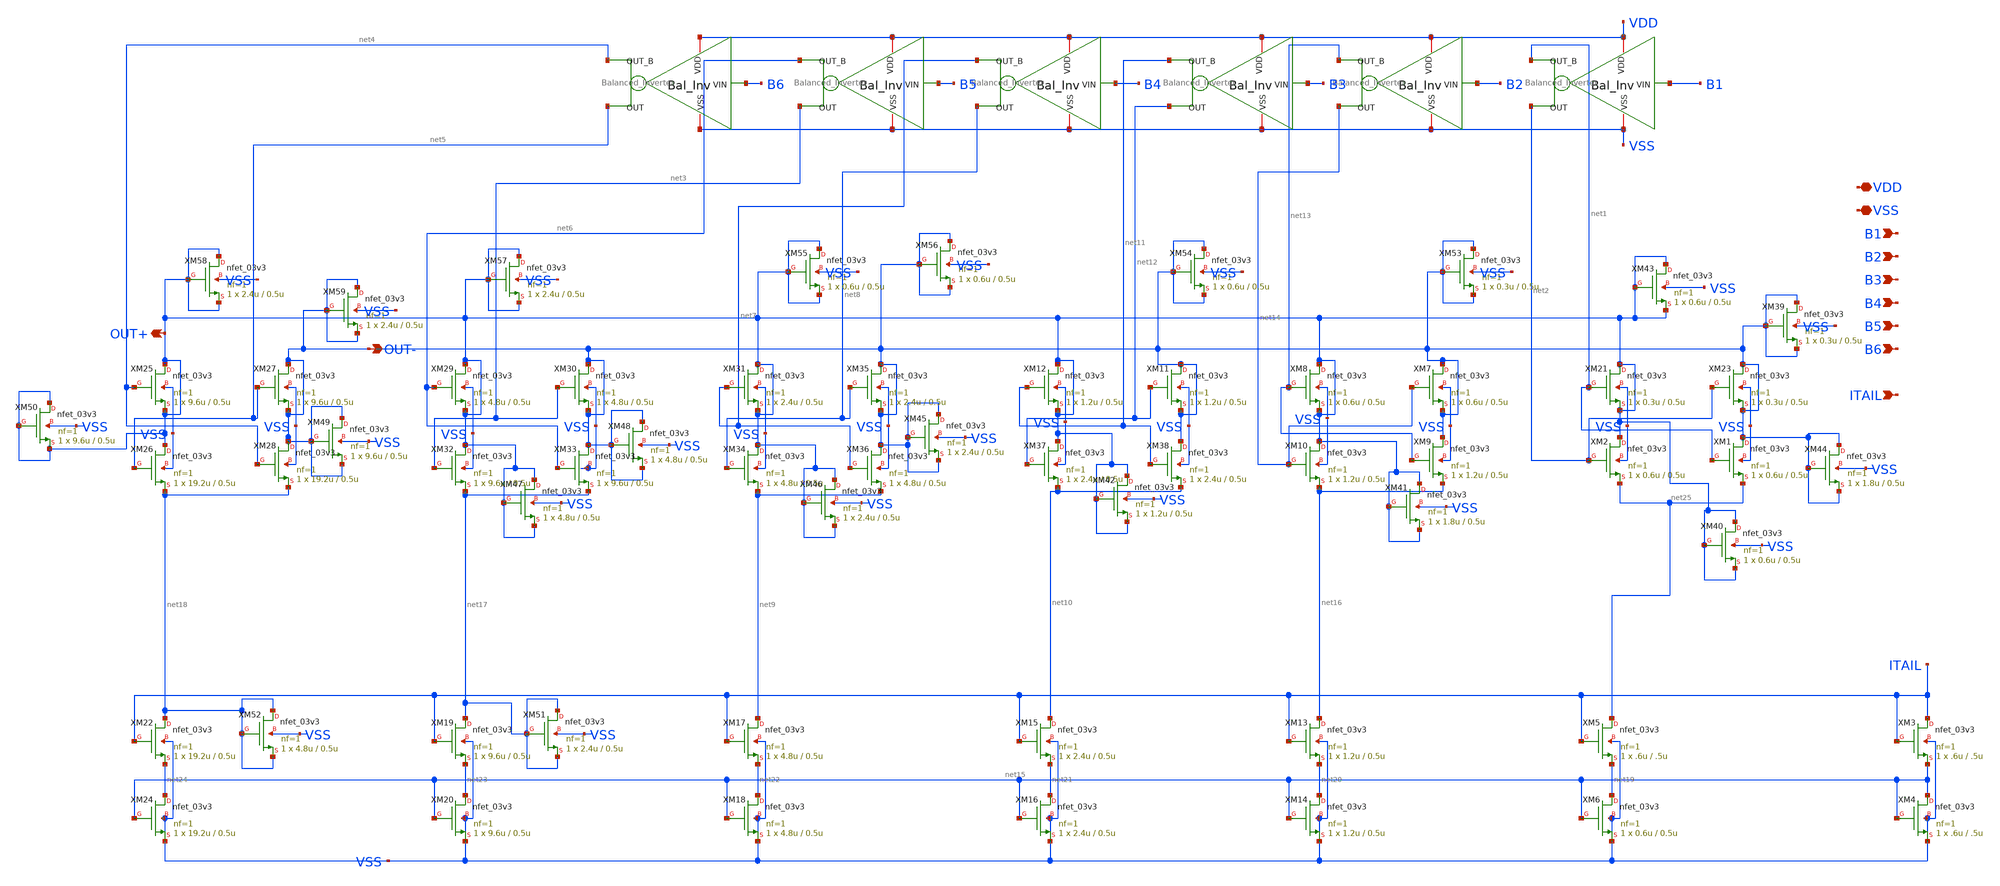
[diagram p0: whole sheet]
** sch_path: DAC_PAKISTAN_01/Pakistan1_Xschem/LSB_V1.sch
**.subckt LSB_V1 VDD VSS B1 B2 B3 B4 B5 B6 ITAIL OUT+ OUT-
*.iopin VDD
*.iopin VSS
*.ipin B1
*.ipin B2
*.ipin B3
*.ipin B4
*.ipin B5
*.ipin B6
*.ipin ITAIL
*.opin OUT+
*.opin OUT-
x1 VDD VSS B1 net1 net2 Balanced_Inverter
x2 VDD VSS B2 net13 net14 Balanced_Inverter
x3 VDD VSS B3 net11 net12 Balanced_Inverter
x4 VDD VSS B4 net7 net8 Balanced_Inverter
x5 VDD VSS B5 net6 net3 Balanced_Inverter
x6 VDD VSS B6 net4 net5 Balanced_Inverter
XM21 OUT+ net1 OUT+ VSS nfet_03v3 L=0.5u W=0.3u nf=1 ad='int((nf+1)/2) * W/nf * 0.18u' as='int((nf+2)/2) * W/nf * 0.18u'
+ pd='2*int((nf+1)/2) * (W/nf + 0.18u)' ps='2*int((nf+2)/2) * (W/nf + 0.18u)' nrd='0.18u / W' nrs='0.18u / W'
+ sa=0 sb=0 sd=0 m=1
XM23 OUT- net2 OUT- VSS nfet_03v3 L=0.5u W=0.3u nf=1 ad='int((nf+1)/2) * W/nf * 0.18u' as='int((nf+2)/2) * W/nf * 0.18u'
+ pd='2*int((nf+1)/2) * (W/nf + 0.18u)' ps='2*int((nf+2)/2) * (W/nf + 0.18u)' nrd='0.18u / W' nrs='0.18u / W'
+ sa=0 sb=0 sd=0 m=1
XM1 OUT- net1 net25 VSS nfet_03v3 L=0.5u W=0.6u nf=1 ad='int((nf+1)/2) * W/nf * 0.18u' as='int((nf+2)/2) * W/nf * 0.18u'
+ pd='2*int((nf+1)/2) * (W/nf + 0.18u)' ps='2*int((nf+2)/2) * (W/nf + 0.18u)' nrd='0.18u / W' nrs='0.18u / W'
+ sa=0 sb=0 sd=0 m=1
XM2 OUT+ net2 net25 VSS nfet_03v3 L=0.5u W=0.6u nf=1 ad='int((nf+1)/2) * W/nf * 0.18u' as='int((nf+2)/2) * W/nf * 0.18u'
+ pd='2*int((nf+1)/2) * (W/nf + 0.18u)' ps='2*int((nf+2)/2) * (W/nf + 0.18u)' nrd='0.18u / W' nrs='0.18u / W'
+ sa=0 sb=0 sd=0 m=1
XM3 ITAIL ITAIL net15 VSS nfet_03v3 L=.5u W=.6u nf=1 ad='int((nf+1)/2) * W/nf * 0.18u' as='int((nf+2)/2) * W/nf * 0.18u'
+ pd='2*int((nf+1)/2) * (W/nf + 0.18u)' ps='2*int((nf+2)/2) * (W/nf + 0.18u)' nrd='0.18u / W' nrs='0.18u / W'
+ sa=0 sb=0 sd=0 m=1
XM4 net15 net15 VSS VSS nfet_03v3 L=.5u W=.6u nf=1 ad='int((nf+1)/2) * W/nf * 0.18u' as='int((nf+2)/2) * W/nf * 0.18u'
+ pd='2*int((nf+1)/2) * (W/nf + 0.18u)' ps='2*int((nf+2)/2) * (W/nf + 0.18u)' nrd='0.18u / W' nrs='0.18u / W'
+ sa=0 sb=0 sd=0 m=1
XM5 net25 ITAIL net19 VSS nfet_03v3 L=.5u W=.6u nf=1 ad='int((nf+1)/2) * W/nf * 0.18u' as='int((nf+2)/2) * W/nf * 0.18u'
+ pd='2*int((nf+1)/2) * (W/nf + 0.18u)' ps='2*int((nf+2)/2) * (W/nf + 0.18u)' nrd='0.18u / W' nrs='0.18u / W'
+ sa=0 sb=0 sd=0 m=1
XM6 net19 net15 VSS VSS nfet_03v3 L=0.5u W=0.6u nf=1 ad='int((nf+1)/2) * W/nf * 0.18u' as='int((nf+2)/2) * W/nf * 0.18u'
+ pd='2*int((nf+1)/2) * (W/nf + 0.18u)' ps='2*int((nf+2)/2) * (W/nf + 0.18u)' nrd='0.18u / W' nrs='0.18u / W'
+ sa=0 sb=0 sd=0 m=1
XM7 OUT- net14 OUT- VSS nfet_03v3 L=0.5u W=0.6u nf=1 ad='int((nf+1)/2) * W/nf * 0.18u' as='int((nf+2)/2) * W/nf * 0.18u'
+ pd='2*int((nf+1)/2) * (W/nf + 0.18u)' ps='2*int((nf+2)/2) * (W/nf + 0.18u)' nrd='0.18u / W' nrs='0.18u / W'
+ sa=0 sb=0 sd=0 m=1
XM8 OUT+ net13 OUT+ VSS nfet_03v3 L=0.5u W=0.6u nf=1 ad='int((nf+1)/2) * W/nf * 0.18u' as='int((nf+2)/2) * W/nf * 0.18u'
+ pd='2*int((nf+1)/2) * (W/nf + 0.18u)' ps='2*int((nf+2)/2) * (W/nf + 0.18u)' nrd='0.18u / W' nrs='0.18u / W'
+ sa=0 sb=0 sd=0 m=1
XM9 OUT- net13 net16 VSS nfet_03v3 L=0.5u W=1.2u nf=1 ad='int((nf+1)/2) * W/nf * 0.18u' as='int((nf+2)/2) * W/nf * 0.18u'
+ pd='2*int((nf+1)/2) * (W/nf + 0.18u)' ps='2*int((nf+2)/2) * (W/nf + 0.18u)' nrd='0.18u / W' nrs='0.18u / W'
+ sa=0 sb=0 sd=0 m=1
XM10 OUT+ net14 net16 VSS nfet_03v3 L=0.5u W=1.2u nf=1 ad='int((nf+1)/2) * W/nf * 0.18u' as='int((nf+2)/2) * W/nf * 0.18u'
+ pd='2*int((nf+1)/2) * (W/nf + 0.18u)' ps='2*int((nf+2)/2) * (W/nf + 0.18u)' nrd='0.18u / W' nrs='0.18u / W'
+ sa=0 sb=0 sd=0 m=1
XM11 OUT- net12 OUT- VSS nfet_03v3 L=0.5u W=1.2u nf=1 ad='int((nf+1)/2) * W/nf * 0.18u' as='int((nf+2)/2) * W/nf * 0.18u'
+ pd='2*int((nf+1)/2) * (W/nf + 0.18u)' ps='2*int((nf+2)/2) * (W/nf + 0.18u)' nrd='0.18u / W' nrs='0.18u / W'
+ sa=0 sb=0 sd=0 m=1
XM12 OUT+ net11 OUT+ VSS nfet_03v3 L=0.5u W=1.2u nf=1 ad='int((nf+1)/2) * W/nf * 0.18u' as='int((nf+2)/2) * W/nf * 0.18u'
+ pd='2*int((nf+1)/2) * (W/nf + 0.18u)' ps='2*int((nf+2)/2) * (W/nf + 0.18u)' nrd='0.18u / W' nrs='0.18u / W'
+ sa=0 sb=0 sd=0 m=1
XM13 net16 ITAIL net20 VSS nfet_03v3 L=0.5u W=1.2u nf=1 ad='int((nf+1)/2) * W/nf * 0.18u' as='int((nf+2)/2) * W/nf * 0.18u'
+ pd='2*int((nf+1)/2) * (W/nf + 0.18u)' ps='2*int((nf+2)/2) * (W/nf + 0.18u)' nrd='0.18u / W' nrs='0.18u / W'
+ sa=0 sb=0 sd=0 m=1
XM14 net20 net15 VSS VSS nfet_03v3 L=0.5u W=1.2u nf=1 ad='int((nf+1)/2) * W/nf * 0.18u' as='int((nf+2)/2) * W/nf * 0.18u'
+ pd='2*int((nf+1)/2) * (W/nf + 0.18u)' ps='2*int((nf+2)/2) * (W/nf + 0.18u)' nrd='0.18u / W' nrs='0.18u / W'
+ sa=0 sb=0 sd=0 m=1
XM15 net10 ITAIL net21 VSS nfet_03v3 L=0.5u W=2.4u nf=1 ad='int((nf+1)/2) * W/nf * 0.18u' as='int((nf+2)/2) * W/nf * 0.18u'
+ pd='2*int((nf+1)/2) * (W/nf + 0.18u)' ps='2*int((nf+2)/2) * (W/nf + 0.18u)' nrd='0.18u / W' nrs='0.18u / W'
+ sa=0 sb=0 sd=0 m=1
XM16 net21 net15 VSS VSS nfet_03v3 L=0.5u W=2.4u nf=1 ad='int((nf+1)/2) * W/nf * 0.18u' as='int((nf+2)/2) * W/nf * 0.18u'
+ pd='2*int((nf+1)/2) * (W/nf + 0.18u)' ps='2*int((nf+2)/2) * (W/nf + 0.18u)' nrd='0.18u / W' nrs='0.18u / W'
+ sa=0 sb=0 sd=0 m=1
XM17 net9 ITAIL net22 VSS nfet_03v3 L=0.5u W=4.8u nf=1 ad='int((nf+1)/2) * W/nf * 0.18u' as='int((nf+2)/2) * W/nf * 0.18u'
+ pd='2*int((nf+1)/2) * (W/nf + 0.18u)' ps='2*int((nf+2)/2) * (W/nf + 0.18u)' nrd='0.18u / W' nrs='0.18u / W'
+ sa=0 sb=0 sd=0 m=1
XM18 net22 net15 VSS VSS nfet_03v3 L=0.5u W=4.8u nf=1 ad='int((nf+1)/2) * W/nf * 0.18u' as='int((nf+2)/2) * W/nf * 0.18u'
+ pd='2*int((nf+1)/2) * (W/nf + 0.18u)' ps='2*int((nf+2)/2) * (W/nf + 0.18u)' nrd='0.18u / W' nrs='0.18u / W'
+ sa=0 sb=0 sd=0 m=1
XM19 net17 ITAIL net23 VSS nfet_03v3 L=0.5u W=9.6u nf=1 ad='int((nf+1)/2) * W/nf * 0.18u' as='int((nf+2)/2) * W/nf * 0.18u'
+ pd='2*int((nf+1)/2) * (W/nf + 0.18u)' ps='2*int((nf+2)/2) * (W/nf + 0.18u)' nrd='0.18u / W' nrs='0.18u / W'
+ sa=0 sb=0 sd=0 m=1
XM20 net23 net15 VSS VSS nfet_03v3 L=0.5u W=9.6u nf=1 ad='int((nf+1)/2) * W/nf * 0.18u' as='int((nf+2)/2) * W/nf * 0.18u'
+ pd='2*int((nf+1)/2) * (W/nf + 0.18u)' ps='2*int((nf+2)/2) * (W/nf + 0.18u)' nrd='0.18u / W' nrs='0.18u / W'
+ sa=0 sb=0 sd=0 m=1
XM22 net18 ITAIL net24 VSS nfet_03v3 L=0.5u W=19.2u nf=1 ad='int((nf+1)/2) * W/nf * 0.18u' as='int((nf+2)/2) * W/nf * 0.18u'
+ pd='2*int((nf+1)/2) * (W/nf + 0.18u)' ps='2*int((nf+2)/2) * (W/nf + 0.18u)' nrd='0.18u / W' nrs='0.18u / W'
+ sa=0 sb=0 sd=0 m=1
XM24 net24 net15 VSS VSS nfet_03v3 L=0.5u W=19.2u nf=1 ad='int((nf+1)/2) * W/nf * 0.18u' as='int((nf+2)/2) * W/nf * 0.18u'
+ pd='2*int((nf+1)/2) * (W/nf + 0.18u)' ps='2*int((nf+2)/2) * (W/nf + 0.18u)' nrd='0.18u / W' nrs='0.18u / W'
+ sa=0 sb=0 sd=0 m=1
XM25 OUT+ net4 OUT+ VSS nfet_03v3 L=0.5u W=9.6u nf=1 ad='int((nf+1)/2) * W/nf * 0.18u' as='int((nf+2)/2) * W/nf * 0.18u'
+ pd='2*int((nf+1)/2) * (W/nf + 0.18u)' ps='2*int((nf+2)/2) * (W/nf + 0.18u)' nrd='0.18u / W' nrs='0.18u / W'
+ sa=0 sb=0 sd=0 m=1
XM26 OUT+ net5 net18 VSS nfet_03v3 L=0.5u W=19.2u nf=1 ad='int((nf+1)/2) * W/nf * 0.18u' as='int((nf+2)/2) * W/nf * 0.18u'
+ pd='2*int((nf+1)/2) * (W/nf + 0.18u)' ps='2*int((nf+2)/2) * (W/nf + 0.18u)' nrd='0.18u / W' nrs='0.18u / W'
+ sa=0 sb=0 sd=0 m=1
XM27 OUT- net5 OUT- VSS nfet_03v3 L=0.5u W=9.6u nf=1 ad='int((nf+1)/2) * W/nf * 0.18u' as='int((nf+2)/2) * W/nf * 0.18u'
+ pd='2*int((nf+1)/2) * (W/nf + 0.18u)' ps='2*int((nf+2)/2) * (W/nf + 0.18u)' nrd='0.18u / W' nrs='0.18u / W'
+ sa=0 sb=0 sd=0 m=1
XM28 OUT- net4 net18 VSS nfet_03v3 L=0.5u W=19.2u nf=1 ad='int((nf+1)/2) * W/nf * 0.18u' as='int((nf+2)/2) * W/nf * 0.18u'
+ pd='2*int((nf+1)/2) * (W/nf + 0.18u)' ps='2*int((nf+2)/2) * (W/nf + 0.18u)' nrd='0.18u / W' nrs='0.18u / W'
+ sa=0 sb=0 sd=0 m=1
XM29 OUT+ net6 OUT+ VSS nfet_03v3 L=0.5u W=4.8u nf=1 ad='int((nf+1)/2) * W/nf * 0.18u' as='int((nf+2)/2) * W/nf * 0.18u'
+ pd='2*int((nf+1)/2) * (W/nf + 0.18u)' ps='2*int((nf+2)/2) * (W/nf + 0.18u)' nrd='0.18u / W' nrs='0.18u / W'
+ sa=0 sb=0 sd=0 m=1
XM30 OUT- net3 OUT- VSS nfet_03v3 L=0.5u W=4.8u nf=1 ad='int((nf+1)/2) * W/nf * 0.18u' as='int((nf+2)/2) * W/nf * 0.18u'
+ pd='2*int((nf+1)/2) * (W/nf + 0.18u)' ps='2*int((nf+2)/2) * (W/nf + 0.18u)' nrd='0.18u / W' nrs='0.18u / W'
+ sa=0 sb=0 sd=0 m=1
XM31 OUT+ net7 OUT+ VSS nfet_03v3 L=0.5u W=2.4u nf=1 ad='int((nf+1)/2) * W/nf * 0.18u' as='int((nf+2)/2) * W/nf * 0.18u'
+ pd='2*int((nf+1)/2) * (W/nf + 0.18u)' ps='2*int((nf+2)/2) * (W/nf + 0.18u)' nrd='0.18u / W' nrs='0.18u / W'
+ sa=0 sb=0 sd=0 m=1
XM32 OUT+ net3 net17 VSS nfet_03v3 L=0.5u W=9.6u nf=1 ad='int((nf+1)/2) * W/nf * 0.18u' as='int((nf+2)/2) * W/nf * 0.18u'
+ pd='2*int((nf+1)/2) * (W/nf + 0.18u)' ps='2*int((nf+2)/2) * (W/nf + 0.18u)' nrd='0.18u / W' nrs='0.18u / W'
+ sa=0 sb=0 sd=0 m=1
XM33 OUT- net6 net17 VSS nfet_03v3 L=0.5u W=9.6u nf=1 ad='int((nf+1)/2) * W/nf * 0.18u' as='int((nf+2)/2) * W/nf * 0.18u'
+ pd='2*int((nf+1)/2) * (W/nf + 0.18u)' ps='2*int((nf+2)/2) * (W/nf + 0.18u)' nrd='0.18u / W' nrs='0.18u / W'
+ sa=0 sb=0 sd=0 m=1
XM34 OUT+ net8 net9 VSS nfet_03v3 L=0.5u W=4.8u nf=1 ad='int((nf+1)/2) * W/nf * 0.18u' as='int((nf+2)/2) * W/nf * 0.18u'
+ pd='2*int((nf+1)/2) * (W/nf + 0.18u)' ps='2*int((nf+2)/2) * (W/nf + 0.18u)' nrd='0.18u / W' nrs='0.18u / W'
+ sa=0 sb=0 sd=0 m=1
XM35 OUT- net8 OUT- VSS nfet_03v3 L=0.5u W=2.4u nf=1 ad='int((nf+1)/2) * W/nf * 0.18u' as='int((nf+2)/2) * W/nf * 0.18u'
+ pd='2*int((nf+1)/2) * (W/nf + 0.18u)' ps='2*int((nf+2)/2) * (W/nf + 0.18u)' nrd='0.18u / W' nrs='0.18u / W'
+ sa=0 sb=0 sd=0 m=1
XM36 OUT- net7 net9 VSS nfet_03v3 L=0.5u W=4.8u nf=1 ad='int((nf+1)/2) * W/nf * 0.18u' as='int((nf+2)/2) * W/nf * 0.18u'
+ pd='2*int((nf+1)/2) * (W/nf + 0.18u)' ps='2*int((nf+2)/2) * (W/nf + 0.18u)' nrd='0.18u / W' nrs='0.18u / W'
+ sa=0 sb=0 sd=0 m=1
XM37 OUT+ net12 net10 VSS nfet_03v3 L=0.5u W=2.4u nf=1 ad='int((nf+1)/2) * W/nf * 0.18u' as='int((nf+2)/2) * W/nf * 0.18u'
+ pd='2*int((nf+1)/2) * (W/nf + 0.18u)' ps='2*int((nf+2)/2) * (W/nf + 0.18u)' nrd='0.18u / W' nrs='0.18u / W'
+ sa=0 sb=0 sd=0 m=1
XM38 OUT- net11 net10 VSS nfet_03v3 L=0.5u W=2.4u nf=1 ad='int((nf+1)/2) * W/nf * 0.18u' as='int((nf+2)/2) * W/nf * 0.18u'
+ pd='2*int((nf+1)/2) * (W/nf + 0.18u)' ps='2*int((nf+2)/2) * (W/nf + 0.18u)' nrd='0.18u / W' nrs='0.18u / W'
+ sa=0 sb=0 sd=0 m=1
XM39 OUT- OUT- OUT- VSS nfet_03v3 L=0.5u W=0.3u nf=1 ad='int((nf+1)/2) * W/nf * 0.18u' as='int((nf+2)/2) * W/nf * 0.18u'
+ pd='2*int((nf+1)/2) * (W/nf + 0.18u)' ps='2*int((nf+2)/2) * (W/nf + 0.18u)' nrd='0.18u / W' nrs='0.18u / W'
+ sa=0 sb=0 sd=0 m=1
XM40 OUT+ OUT+ OUT+ VSS nfet_03v3 L=0.5u W=0.6u nf=1 ad='int((nf+1)/2) * W/nf * 0.18u' as='int((nf+2)/2) * W/nf * 0.18u'
+ pd='2*int((nf+1)/2) * (W/nf + 0.18u)' ps='2*int((nf+2)/2) * (W/nf + 0.18u)' nrd='0.18u / W' nrs='0.18u / W'
+ sa=0 sb=0 sd=0 m=1
XM41 OUT+ OUT+ OUT+ VSS nfet_03v3 L=0.5u W=1.8u nf=1 ad='int((nf+1)/2) * W/nf * 0.18u' as='int((nf+2)/2) * W/nf * 0.18u'
+ pd='2*int((nf+1)/2) * (W/nf + 0.18u)' ps='2*int((nf+2)/2) * (W/nf + 0.18u)' nrd='0.18u / W' nrs='0.18u / W'
+ sa=0 sb=0 sd=0 m=1
XM42 OUT+ OUT+ OUT+ VSS nfet_03v3 L=0.5u W=1.2u nf=1 ad='int((nf+1)/2) * W/nf * 0.18u' as='int((nf+2)/2) * W/nf * 0.18u'
+ pd='2*int((nf+1)/2) * (W/nf + 0.18u)' ps='2*int((nf+2)/2) * (W/nf + 0.18u)' nrd='0.18u / W' nrs='0.18u / W'
+ sa=0 sb=0 sd=0 m=1
XM43 OUT+ OUT+ OUT+ VSS nfet_03v3 L=0.5u W=0.6u nf=1 ad='int((nf+1)/2) * W/nf * 0.18u' as='int((nf+2)/2) * W/nf * 0.18u'
+ pd='2*int((nf+1)/2) * (W/nf + 0.18u)' ps='2*int((nf+2)/2) * (W/nf + 0.18u)' nrd='0.18u / W' nrs='0.18u / W'
+ sa=0 sb=0 sd=0 m=1
XM44 OUT- OUT- OUT- VSS nfet_03v3 L=0.5u W=1.8u nf=1 ad='int((nf+1)/2) * W/nf * 0.18u' as='int((nf+2)/2) * W/nf * 0.18u'
+ pd='2*int((nf+1)/2) * (W/nf + 0.18u)' ps='2*int((nf+2)/2) * (W/nf + 0.18u)' nrd='0.18u / W' nrs='0.18u / W'
+ sa=0 sb=0 sd=0 m=1
XM45 OUT- OUT- OUT- VSS nfet_03v3 L=0.5u W=2.4u nf=1 ad='int((nf+1)/2) * W/nf * 0.18u' as='int((nf+2)/2) * W/nf * 0.18u'
+ pd='2*int((nf+1)/2) * (W/nf + 0.18u)' ps='2*int((nf+2)/2) * (W/nf + 0.18u)' nrd='0.18u / W' nrs='0.18u / W'
+ sa=0 sb=0 sd=0 m=1
XM46 OUT+ OUT+ OUT+ VSS nfet_03v3 L=0.5u W=2.4u nf=1 ad='int((nf+1)/2) * W/nf * 0.18u' as='int((nf+2)/2) * W/nf * 0.18u'
+ pd='2*int((nf+1)/2) * (W/nf + 0.18u)' ps='2*int((nf+2)/2) * (W/nf + 0.18u)' nrd='0.18u / W' nrs='0.18u / W'
+ sa=0 sb=0 sd=0 m=1
XM47 OUT+ OUT+ OUT+ VSS nfet_03v3 L=0.5u W=4.8u nf=1 ad='int((nf+1)/2) * W/nf * 0.18u' as='int((nf+2)/2) * W/nf * 0.18u'
+ pd='2*int((nf+1)/2) * (W/nf + 0.18u)' ps='2*int((nf+2)/2) * (W/nf + 0.18u)' nrd='0.18u / W' nrs='0.18u / W'
+ sa=0 sb=0 sd=0 m=1
XM48 OUT- OUT- OUT- VSS nfet_03v3 L=0.5u W=4.8u nf=1 ad='int((nf+1)/2) * W/nf * 0.18u' as='int((nf+2)/2) * W/nf * 0.18u'
+ pd='2*int((nf+1)/2) * (W/nf + 0.18u)' ps='2*int((nf+2)/2) * (W/nf + 0.18u)' nrd='0.18u / W' nrs='0.18u / W'
+ sa=0 sb=0 sd=0 m=1
XM49 OUT- OUT- OUT- VSS nfet_03v3 L=0.5u W=9.6u nf=1 ad='int((nf+1)/2) * W/nf * 0.18u' as='int((nf+2)/2) * W/nf * 0.18u'
+ pd='2*int((nf+1)/2) * (W/nf + 0.18u)' ps='2*int((nf+2)/2) * (W/nf + 0.18u)' nrd='0.18u / W' nrs='0.18u / W'
+ sa=0 sb=0 sd=0 m=1
XM50 OUT+ OUT+ OUT+ VSS nfet_03v3 L=0.5u W=9.6u nf=1 ad='int((nf+1)/2) * W/nf * 0.18u' as='int((nf+2)/2) * W/nf * 0.18u'
+ pd='2*int((nf+1)/2) * (W/nf + 0.18u)' ps='2*int((nf+2)/2) * (W/nf + 0.18u)' nrd='0.18u / W' nrs='0.18u / W'
+ sa=0 sb=0 sd=0 m=1
XM51 net17 net17 net17 VSS nfet_03v3 L=0.5u W=2.4u nf=1 ad='int((nf+1)/2) * W/nf * 0.18u' as='int((nf+2)/2) * W/nf * 0.18u'
+ pd='2*int((nf+1)/2) * (W/nf + 0.18u)' ps='2*int((nf+2)/2) * (W/nf + 0.18u)' nrd='0.18u / W' nrs='0.18u / W'
+ sa=0 sb=0 sd=0 m=1
XM52 net18 net18 net18 VSS nfet_03v3 L=0.5u W=4.8u nf=1 ad='int((nf+1)/2) * W/nf * 0.18u' as='int((nf+2)/2) * W/nf * 0.18u'
+ pd='2*int((nf+1)/2) * (W/nf + 0.18u)' ps='2*int((nf+2)/2) * (W/nf + 0.18u)' nrd='0.18u / W' nrs='0.18u / W'
+ sa=0 sb=0 sd=0 m=1
XM53 OUT- OUT- OUT- VSS nfet_03v3 L=0.5u W=0.3u nf=1 ad='int((nf+1)/2) * W/nf * 0.18u' as='int((nf+2)/2) * W/nf * 0.18u'
+ pd='2*int((nf+1)/2) * (W/nf + 0.18u)' ps='2*int((nf+2)/2) * (W/nf + 0.18u)' nrd='0.18u / W' nrs='0.18u / W'
+ sa=0 sb=0 sd=0 m=1
XM54 OUT- OUT- OUT- VSS nfet_03v3 L=0.5u W=0.6u nf=1 ad='int((nf+1)/2) * W/nf * 0.18u' as='int((nf+2)/2) * W/nf * 0.18u'
+ pd='2*int((nf+1)/2) * (W/nf + 0.18u)' ps='2*int((nf+2)/2) * (W/nf + 0.18u)' nrd='0.18u / W' nrs='0.18u / W'
+ sa=0 sb=0 sd=0 m=1
XM55 OUT+ OUT+ OUT+ VSS nfet_03v3 L=0.5u W=0.6u nf=1 ad='int((nf+1)/2) * W/nf * 0.18u' as='int((nf+2)/2) * W/nf * 0.18u'
+ pd='2*int((nf+1)/2) * (W/nf + 0.18u)' ps='2*int((nf+2)/2) * (W/nf + 0.18u)' nrd='0.18u / W' nrs='0.18u / W'
+ sa=0 sb=0 sd=0 m=1
XM56 OUT- OUT- OUT- VSS nfet_03v3 L=0.5u W=0.6u nf=1 ad='int((nf+1)/2) * W/nf * 0.18u' as='int((nf+2)/2) * W/nf * 0.18u'
+ pd='2*int((nf+1)/2) * (W/nf + 0.18u)' ps='2*int((nf+2)/2) * (W/nf + 0.18u)' nrd='0.18u / W' nrs='0.18u / W'
+ sa=0 sb=0 sd=0 m=1
XM57 OUT+ OUT+ OUT+ VSS nfet_03v3 L=0.5u W=2.4u nf=1 ad='int((nf+1)/2) * W/nf * 0.18u' as='int((nf+2)/2) * W/nf * 0.18u'
+ pd='2*int((nf+1)/2) * (W/nf + 0.18u)' ps='2*int((nf+2)/2) * (W/nf + 0.18u)' nrd='0.18u / W' nrs='0.18u / W'
+ sa=0 sb=0 sd=0 m=1
XM58 OUT+ OUT+ OUT+ VSS nfet_03v3 L=0.5u W=2.4u nf=1 ad='int((nf+1)/2) * W/nf * 0.18u' as='int((nf+2)/2) * W/nf * 0.18u'
+ pd='2*int((nf+1)/2) * (W/nf + 0.18u)' ps='2*int((nf+2)/2) * (W/nf + 0.18u)' nrd='0.18u / W' nrs='0.18u / W'
+ sa=0 sb=0 sd=0 m=1
XM59 OUT- OUT- OUT- VSS nfet_03v3 L=0.5u W=2.4u nf=1 ad='int((nf+1)/2) * W/nf * 0.18u' as='int((nf+2)/2) * W/nf * 0.18u'
+ pd='2*int((nf+1)/2) * (W/nf + 0.18u)' ps='2*int((nf+2)/2) * (W/nf + 0.18u)' nrd='0.18u / W' nrs='0.18u / W'
+ sa=0 sb=0 sd=0 m=1
**.ends

* expanding   symbol:  Balanced_Inverter.sym # of pins=5
** sym_path: DAC_PAKISTAN_01/Pakistan1_Xschem/Balanced_Inverter.sym
** sch_path: DAC_PAKISTAN_01/Pakistan1_Xschem/Balanced_Inverter.sch
.subckt Balanced_Inverter VDD VSS VIN OUT_B OUT
*.iopin VSS
*.ipin VIN
*.opin OUT_B
*.iopin VDD
*.opin OUT
XM1 OUT_B VIN VSS VSS nfet_03v3 L=0.28u W=0.22u nf=1 ad='int((nf+1)/2) * W/nf * 0.18u' as='int((nf+2)/2) * W/nf * 0.18u'
+ pd='2*int((nf+1)/2) * (W/nf + 0.18u)' ps='2*int((nf+2)/2) * (W/nf + 0.18u)' nrd='0.18u / W' nrs='0.18u / W'
+ sa=0 sb=0 sd=0 m=1
XM2 OUT_B OUT VDD VDD pfet_03v3 L=0.28u W=0.22u nf=1 ad='int((nf+1)/2) * W/nf * 0.18u' as='int((nf+2)/2) * W/nf * 0.18u'
+ pd='2*int((nf+1)/2) * (W/nf + 0.18u)' ps='2*int((nf+2)/2) * (W/nf + 0.18u)' nrd='0.18u / W' nrs='0.18u / W'
+ sa=0 sb=0 sd=0 m=1
XM3 OUT net1 VSS VSS nfet_03v3 L=0.28u W=0.22u nf=1 ad='int((nf+1)/2) * W/nf * 0.18u' as='int((nf+2)/2) * W/nf * 0.18u'
+ pd='2*int((nf+1)/2) * (W/nf + 0.18u)' ps='2*int((nf+2)/2) * (W/nf + 0.18u)' nrd='0.18u / W' nrs='0.18u / W'
+ sa=0 sb=0 sd=0 m=1
XM4 OUT OUT_B VDD VDD pfet_03v3 L=0.28u W=0.22u nf=1 ad='int((nf+1)/2) * W/nf * 0.18u' as='int((nf+2)/2) * W/nf * 0.18u'
+ pd='2*int((nf+1)/2) * (W/nf + 0.18u)' ps='2*int((nf+2)/2) * (W/nf + 0.18u)' nrd='0.18u / W' nrs='0.18u / W'
+ sa=0 sb=0 sd=0 m=1
x1 VSS VDD net1 VIN GF_INV
.ends


* expanding   symbol:  GF_INV.sym # of pins=4
** sym_path: GF_INV.sym
** sch_path: GF_INV.sch
.subckt GF_INV VSS VDD OUT IN
*.iopin VDD
*.iopin VSS
*.ipin IN
*.opin OUT
XM1 OUT IN VSS VSS nfet_03v3 L=0.28u W=0.25u nf=1 ad='int((nf+1)/2) * W/nf * 0.18u' as='int((nf+2)/2) * W/nf * 0.18u'
+ pd='2*int((nf+1)/2) * (W/nf + 0.18u)' ps='2*int((nf+2)/2) * (W/nf + 0.18u)' nrd='0.18u / W' nrs='0.18u / W'
+ sa=0 sb=0 sd=0 m=1
XM2 OUT IN VDD VDD pfet_03v3 L=0.28u W=0.5u nf=1 ad='int((nf+1)/2) * W/nf * 0.18u' as='int((nf+2)/2) * W/nf * 0.18u'
+ pd='2*int((nf+1)/2) * (W/nf + 0.18u)' ps='2*int((nf+2)/2) * (W/nf + 0.18u)' nrd='0.18u / W' nrs='0.18u / W'
+ sa=0 sb=0 sd=0 m=1
.ends

.end
